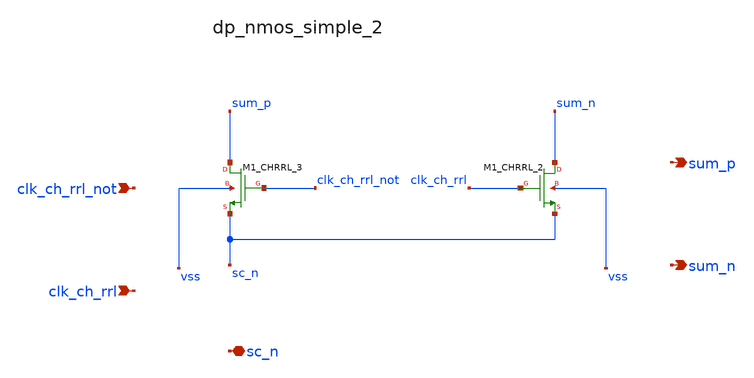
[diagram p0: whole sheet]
** sch_path: analog-db/raw/sup_003_rrl_sc_integrator/hier/blocks/dp_nmos_simple_2.sch
**.subckt dp_nmos_simple_2 clk_ch_rrl_not clk_ch_rrl sc_n sum_p sum_n
*.ipin clk_ch_rrl_not
*.ipin clk_ch_rrl
*.iopin sc_n
*.opin sum_p
*.opin sum_n
XM1_CHRRL_2 sum_n clk_ch_rrl sc_n vss sg13_lv_nmos w=x_dut_xm1_chrrl_2_w l=x_dut_xm1_chrrl_2_l ng=1
+ m=x_dut_xm1_chrrl_2_m
XM1_CHRRL_3 sum_p clk_ch_rrl_not sc_n vss sg13_lv_nmos w=x_dut_xm1_chrrl_3_w l=x_dut_xm1_chrrl_3_l
+ ng=1 m=x_dut_xm1_chrrl_3_m
**.ends
.end
